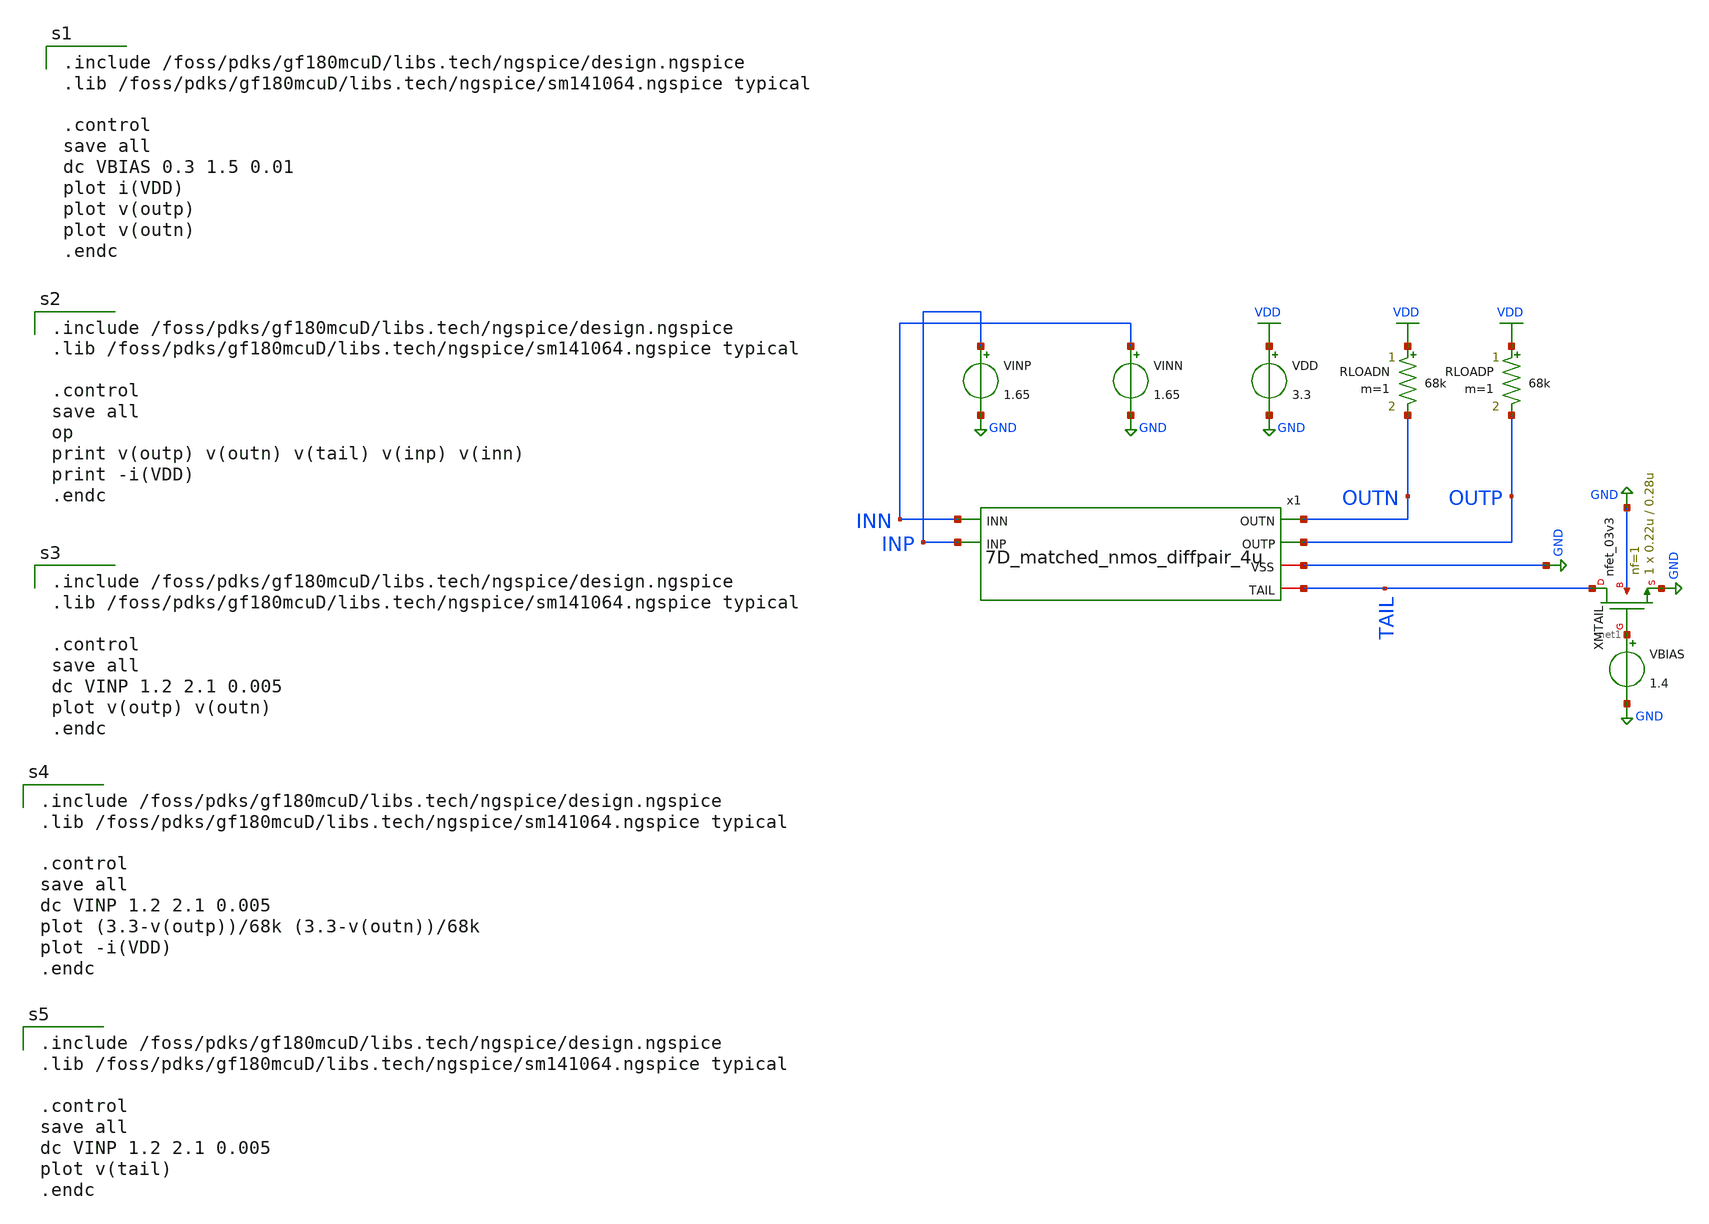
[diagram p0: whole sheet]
** sch_path: designs/libs/tb_matchmaker/tb_7D_matched_nmos_diffpair_4u/tb_7D_matched_nmos_diffpair_4u.sch
**.subckt tb_7D_matched_nmos_diffpair_4u
x1 OUTN OUTP INN INP GND TAIL 7D_matched_nmos_diffpair_4u
VDD VDD GND 3.3
VINN INN GND 1.65
VINP INP GND 1.65
RLOADN VDD OUTN 68k m=1
RLOADP VDD OUTP 68k m=1
XMTAIL TAIL net1 GND GND nfet_03v3 L=0.28u W=0.22u nf=1 ad='int((nf+1)/2) * W/nf * 0.18u' as='int((nf+2)/2) * W/nf * 0.18u'
+ pd='2*int((nf+1)/2) * (W/nf + 0.18u)' ps='2*int((nf+2)/2) * (W/nf + 0.18u)' nrd='0.18u / W' nrs='0.18u / W'
+ sa=0 sb=0 sd=0 m=1
VBIAS net1 GND 1.4
**** begin user architecture code

.include /foss/pdks/gf180mcuD/libs.tech/ngspice/design.ngspice
.lib /foss/pdks/gf180mcuD/libs.tech/ngspice/sm141064.ngspice typical

.control
save all
op
print v(outp) v(outn) v(tail) v(inp) v(inn)
print -i(VDD)
.endc


.include /foss/pdks/gf180mcuD/libs.tech/ngspice/design.ngspice
.lib /foss/pdks/gf180mcuD/libs.tech/ngspice/sm141064.ngspice typical

.control
save all
dc VBIAS 0.3 1.5 0.01
plot i(VDD)
plot v(outp)
plot v(outn)
.endc


.include /foss/pdks/gf180mcuD/libs.tech/ngspice/design.ngspice
.lib /foss/pdks/gf180mcuD/libs.tech/ngspice/sm141064.ngspice typical

.control
save all
dc VINP 1.2 2.1 0.005
plot v(outp) v(outn)
.endc


.include /foss/pdks/gf180mcuD/libs.tech/ngspice/design.ngspice
.lib /foss/pdks/gf180mcuD/libs.tech/ngspice/sm141064.ngspice typical

.control
save all
dc VINP 1.2 2.1 0.005
plot (3.3-v(outp))/68k (3.3-v(outn))/68k
plot -i(VDD)
.endc


.include /foss/pdks/gf180mcuD/libs.tech/ngspice/design.ngspice
.lib /foss/pdks/gf180mcuD/libs.tech/ngspice/sm141064.ngspice typical

.control
save all
dc VINP 1.2 2.1 0.005
plot v(tail)
.endc

**** end user architecture code
**.ends
.GLOBAL VDD
.GLOBAL GND
.end
